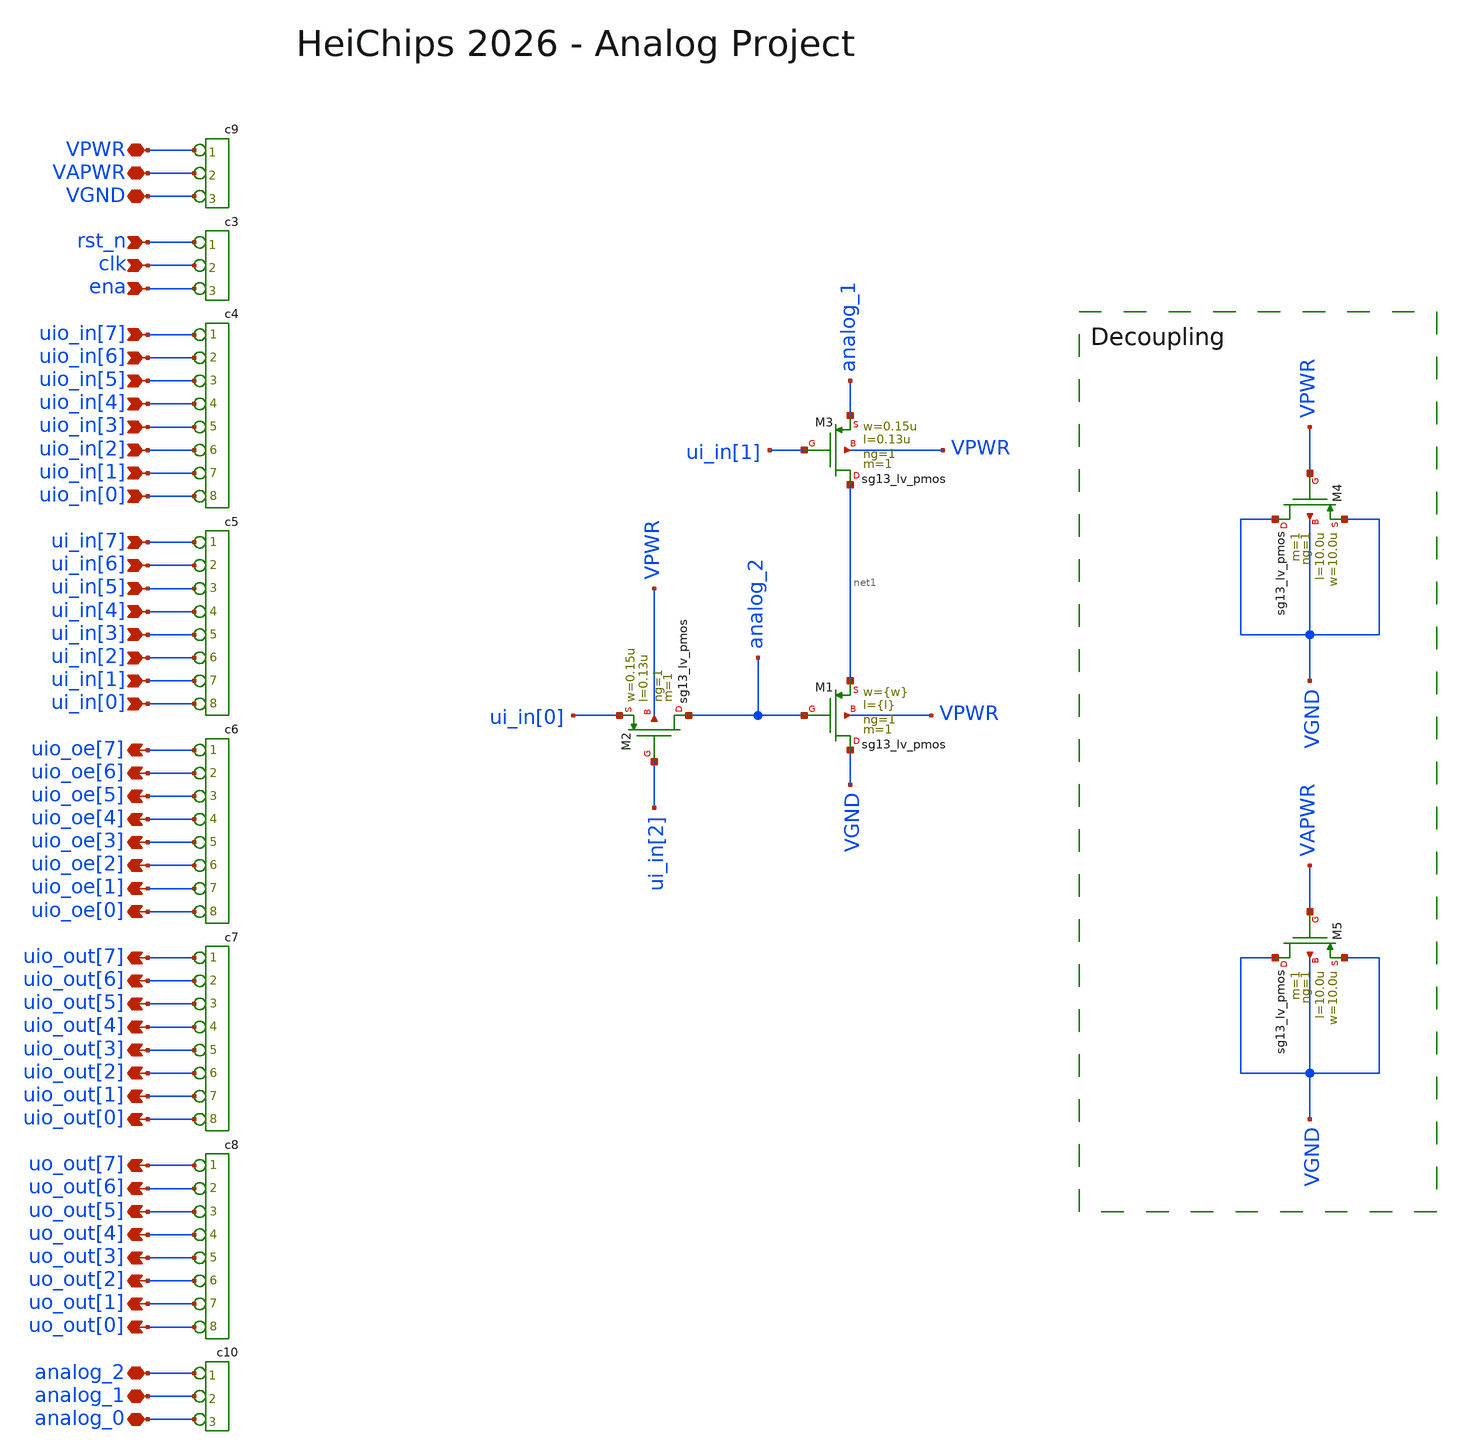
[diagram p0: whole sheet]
** sch_path: macros/heichips26_analog_project/schematic/xschem/heichips26_analog_project.sch
**.subckt heichips26_analog_project rst_n clk ena uio_in[7] ui_in[7] uio_oe[7] uio_oe[6] uio_oe[5]
*+ uio_oe[4] uio_oe[3] uio_oe[2] uio_oe[1] uio_oe[0] uio_out[7] uio_out[6] uio_out[5] uio_out[4] uio_out[3]
*+ uio_out[2] uio_out[1] uio_out[0] uo_out[7] uo_out[6] uo_out[5] uo_out[4] uo_out[3] uo_out[2] uo_out[1]
*+ uo_out[0] VPWR VGND VAPWR ui_in[6] ui_in[5] ui_in[4] ui_in[3] ui_in[2] ui_in[1] ui_in[0] uio_in[6] uio_in[5]
*+ uio_in[4] uio_in[3] uio_in[2] uio_in[1] uio_in[0] analog_2 analog_1 analog_0
*.ipin rst_n
*.ipin clk
*.ipin ena
*.ipin uio_in[7]
*.ipin ui_in[7]
*.opin uio_oe[7]
*.opin uio_oe[6]
*.opin uio_oe[5]
*.opin uio_oe[4]
*.opin uio_oe[3]
*.opin uio_oe[2]
*.opin uio_oe[1]
*.opin uio_oe[0]
*.opin uio_out[7]
*.opin uio_out[6]
*.opin uio_out[5]
*.opin uio_out[4]
*.opin uio_out[3]
*.opin uio_out[2]
*.opin uio_out[1]
*.opin uio_out[0]
*.opin uo_out[7]
*.opin uo_out[6]
*.opin uo_out[5]
*.opin uo_out[4]
*.opin uo_out[3]
*.opin uo_out[2]
*.opin uo_out[1]
*.opin uo_out[0]
*.iopin VPWR
*.iopin VGND
*.iopin VAPWR
*.ipin ui_in[6]
*.ipin ui_in[5]
*.ipin ui_in[4]
*.ipin ui_in[3]
*.ipin ui_in[2]
*.ipin ui_in[1]
*.ipin ui_in[0]
*.ipin uio_in[6]
*.ipin uio_in[5]
*.ipin uio_in[4]
*.ipin uio_in[3]
*.ipin uio_in[2]
*.ipin uio_in[1]
*.ipin uio_in[0]
*.iopin analog_2
*.iopin analog_1
*.iopin analog_0
*connector(3,1) ?1 rst_n ?1 clk ?1 ena
*connector(8,1) ?1 uio_in[7] ?1 uio_in[6] ?1 uio_in[5] ?1 uio_in[4] ?1 uio_in[3] ?1 uio_in[2] ?1
*+ uio_in[1] ?1 uio_in[0]
*connector(8,1) ?1 ui_in[7] ?1 ui_in[6] ?1 ui_in[5] ?1 ui_in[4] ?1 ui_in[3] ?1 ui_in[2] ?1 ui_in[1]
*+ ?1 ui_in[0]
*connector(8,1) ?1 uio_oe[7] ?1 uio_oe[6] ?1 uio_oe[5] ?1 uio_oe[4] ?1 uio_oe[3] ?1 uio_oe[2] ?1
*+ uio_oe[1] ?1 uio_oe[0]
*connector(8,1) ?1 uio_out[7] ?1 uio_out[6] ?1 uio_out[5] ?1 uio_out[4] ?1 uio_out[3] ?1 uio_out[2]
*+ ?1 uio_out[1] ?1 uio_out[0]
*connector(8,1) ?1 uo_out[7] ?1 uo_out[6] ?1 uo_out[5] ?1 uo_out[4] ?1 uo_out[3] ?1 uo_out[2] ?1
*+ uo_out[1] ?1 uo_out[0]
*connector(3,1) ?1 VPWR ?1 VAPWR ?1 VGND
*connector(3,1) ?1 analog_2 ?1 analog_1 ?1 analog_0
XM4 VGND VPWR VGND VGND sg13_lv_pmos w=10.0u l=10.0u ng=1 m=1 mm_ok=1
XM5 VGND VAPWR VGND VGND sg13_lv_pmos w=10.0u l=10.0u ng=1 m=1 mm_ok=1
XM2 analog_2 ui_in[2] ui_in[0] VPWR sg13_lv_pmos w=0.15u l=0.13u ng=1 m=1 mm_ok=1
XM3 net1 ui_in[1] analog_1 VPWR sg13_lv_pmos w=0.15u l=0.13u ng=1 m=1 mm_ok=1
XM1 VGND analog_2 net1 VPWR sg13_lv_pmos w={w} l={l} ng=1 m=1 mm_ok=1
**.ends
.end
